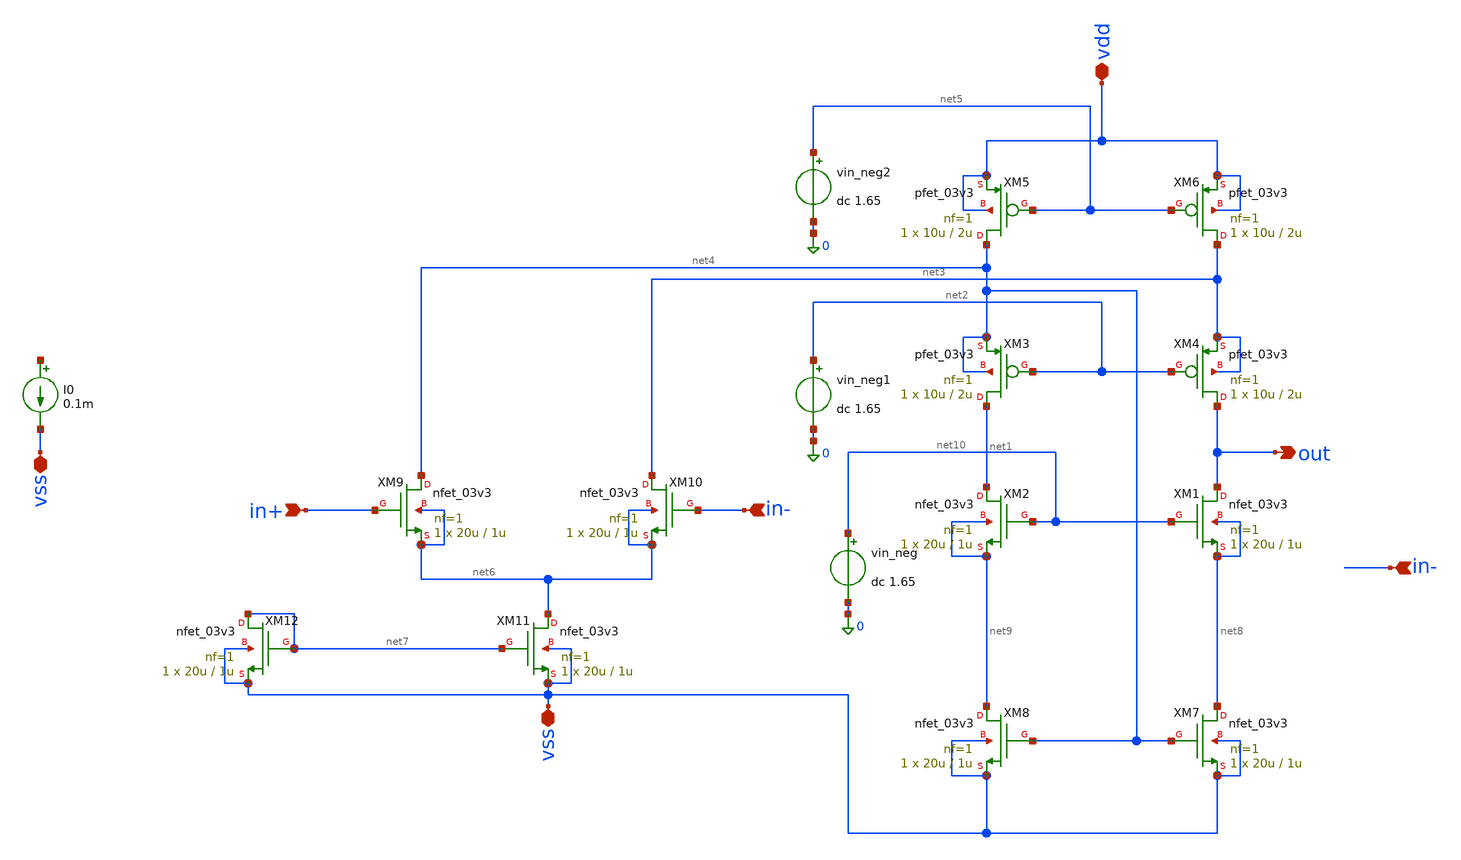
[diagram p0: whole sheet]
** sch_path: General/ADC/OTA/Folded Cascode OP.sch
**.subckt Folded Cascode OP out vss in+ in- vss vdd in-
*.opin out
*.iopin vss
*.ipin in+
*.ipin in-
*.iopin vss
*.iopin vdd
*.ipin in-
XM1 out net10 net8 net8 nfet_03v3 L=1u W=20u nf=1 ad='int((nf+1)/2) * W/nf * 0.18u' as='int((nf+2)/2) * W/nf * 0.18u'
+ pd='2*int((nf+1)/2) * (W/nf + 0.18u)' ps='2*int((nf+2)/2) * (W/nf + 0.18u)' nrd='0.18u / W' nrs='0.18u / W'
+ sa=0 sb=0 sd=0 m=1
XM2 net1 net10 net9 net9 nfet_03v3 L=1u W=20u nf=1 ad='int((nf+1)/2) * W/nf * 0.18u' as='int((nf+2)/2) * W/nf * 0.18u'
+ pd='2*int((nf+1)/2) * (W/nf + 0.18u)' ps='2*int((nf+2)/2) * (W/nf + 0.18u)' nrd='0.18u / W' nrs='0.18u / W'
+ sa=0 sb=0 sd=0 m=1
XM3 net1 net2 net4 net4 pfet_03v3 L=2u W=10u nf=1 ad='int((nf+1)/2) * W/nf * 0.18u' as='int((nf+2)/2) * W/nf * 0.18u'
+ pd='2*int((nf+1)/2) * (W/nf + 0.18u)' ps='2*int((nf+2)/2) * (W/nf + 0.18u)' nrd='0.18u / W' nrs='0.18u / W'
+ sa=0 sb=0 sd=0 m=1
XM4 out net2 net3 net3 pfet_03v3 L=2u W=10u nf=1 ad='int((nf+1)/2) * W/nf * 0.18u' as='int((nf+2)/2) * W/nf * 0.18u'
+ pd='2*int((nf+1)/2) * (W/nf + 0.18u)' ps='2*int((nf+2)/2) * (W/nf + 0.18u)' nrd='0.18u / W' nrs='0.18u / W'
+ sa=0 sb=0 sd=0 m=1
XM5 net4 net5 vdd vdd pfet_03v3 L=2u W=10u nf=1 ad='int((nf+1)/2) * W/nf * 0.18u' as='int((nf+2)/2) * W/nf * 0.18u'
+ pd='2*int((nf+1)/2) * (W/nf + 0.18u)' ps='2*int((nf+2)/2) * (W/nf + 0.18u)' nrd='0.18u / W' nrs='0.18u / W'
+ sa=0 sb=0 sd=0 m=1
XM6 net3 net5 vdd vdd pfet_03v3 L=2u W=10u nf=1 ad='int((nf+1)/2) * W/nf * 0.18u' as='int((nf+2)/2) * W/nf * 0.18u'
+ pd='2*int((nf+1)/2) * (W/nf + 0.18u)' ps='2*int((nf+2)/2) * (W/nf + 0.18u)' nrd='0.18u / W' nrs='0.18u / W'
+ sa=0 sb=0 sd=0 m=1
XM9 net4 in+ net6 net6 nfet_03v3 L=1u W=20u nf=1 ad='int((nf+1)/2) * W/nf * 0.18u' as='int((nf+2)/2) * W/nf * 0.18u'
+ pd='2*int((nf+1)/2) * (W/nf + 0.18u)' ps='2*int((nf+2)/2) * (W/nf + 0.18u)' nrd='0.18u / W' nrs='0.18u / W'
+ sa=0 sb=0 sd=0 m=1
XM10 net3 in- net6 net6 nfet_03v3 L=1u W=20u nf=1 ad='int((nf+1)/2) * W/nf * 0.18u' as='int((nf+2)/2) * W/nf * 0.18u'
+ pd='2*int((nf+1)/2) * (W/nf + 0.18u)' ps='2*int((nf+2)/2) * (W/nf + 0.18u)' nrd='0.18u / W' nrs='0.18u / W'
+ sa=0 sb=0 sd=0 m=1
XM11 net6 net7 vss vss nfet_03v3 L=1u W=20u nf=1 ad='int((nf+1)/2) * W/nf * 0.18u' as='int((nf+2)/2) * W/nf * 0.18u'
+ pd='2*int((nf+1)/2) * (W/nf + 0.18u)' ps='2*int((nf+2)/2) * (W/nf + 0.18u)' nrd='0.18u / W' nrs='0.18u / W'
+ sa=0 sb=0 sd=0 m=1
XM12 net7 net7 vss vss nfet_03v3 L=1u W=20u nf=1 ad='int((nf+1)/2) * W/nf * 0.18u' as='int((nf+2)/2) * W/nf * 0.18u'
+ pd='2*int((nf+1)/2) * (W/nf + 0.18u)' ps='2*int((nf+2)/2) * (W/nf + 0.18u)' nrd='0.18u / W' nrs='0.18u / W'
+ sa=0 sb=0 sd=0 m=1
I0 net11 vss 0.1m
vin_neg net10 0 dc 1.65
vin_neg1 net2 0 dc 1.65
vin_neg2 net5 0 dc 1.65
XM7 net8 net4 vss vss nfet_03v3 L=1u W=20u nf=1 ad='int((nf+1)/2) * W/nf * 0.18u' as='int((nf+2)/2) * W/nf * 0.18u'
+ pd='2*int((nf+1)/2) * (W/nf + 0.18u)' ps='2*int((nf+2)/2) * (W/nf + 0.18u)' nrd='0.18u / W' nrs='0.18u / W'
+ sa=0 sb=0 sd=0 m=1
XM8 net9 net4 vss vss nfet_03v3 L=1u W=20u nf=1 ad='int((nf+1)/2) * W/nf * 0.18u' as='int((nf+2)/2) * W/nf * 0.18u'
+ pd='2*int((nf+1)/2) * (W/nf + 0.18u)' ps='2*int((nf+2)/2) * (W/nf + 0.18u)' nrd='0.18u / W' nrs='0.18u / W'
+ sa=0 sb=0 sd=0 m=1
**.ends
.end
